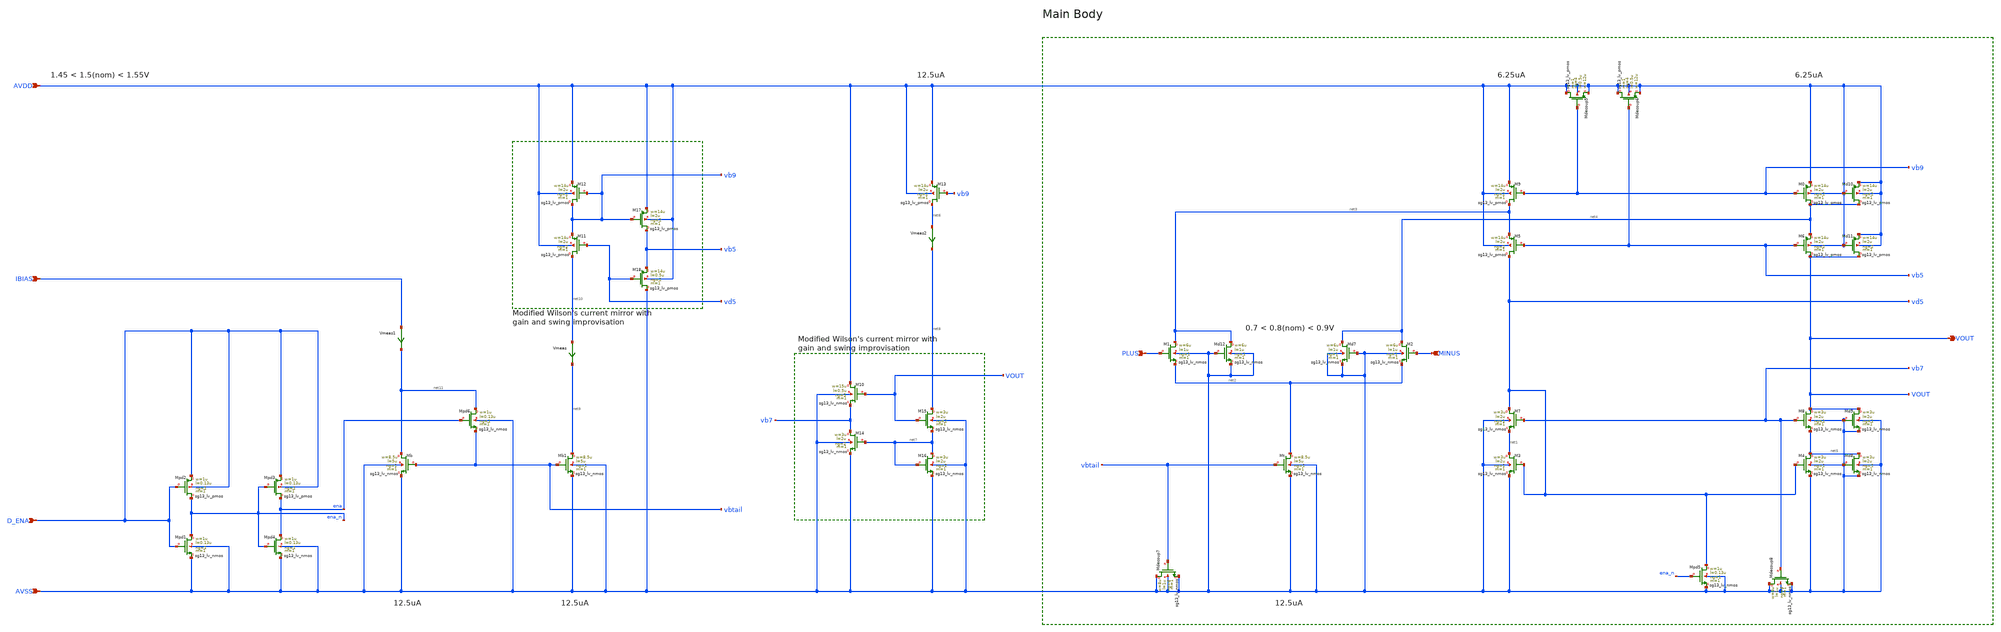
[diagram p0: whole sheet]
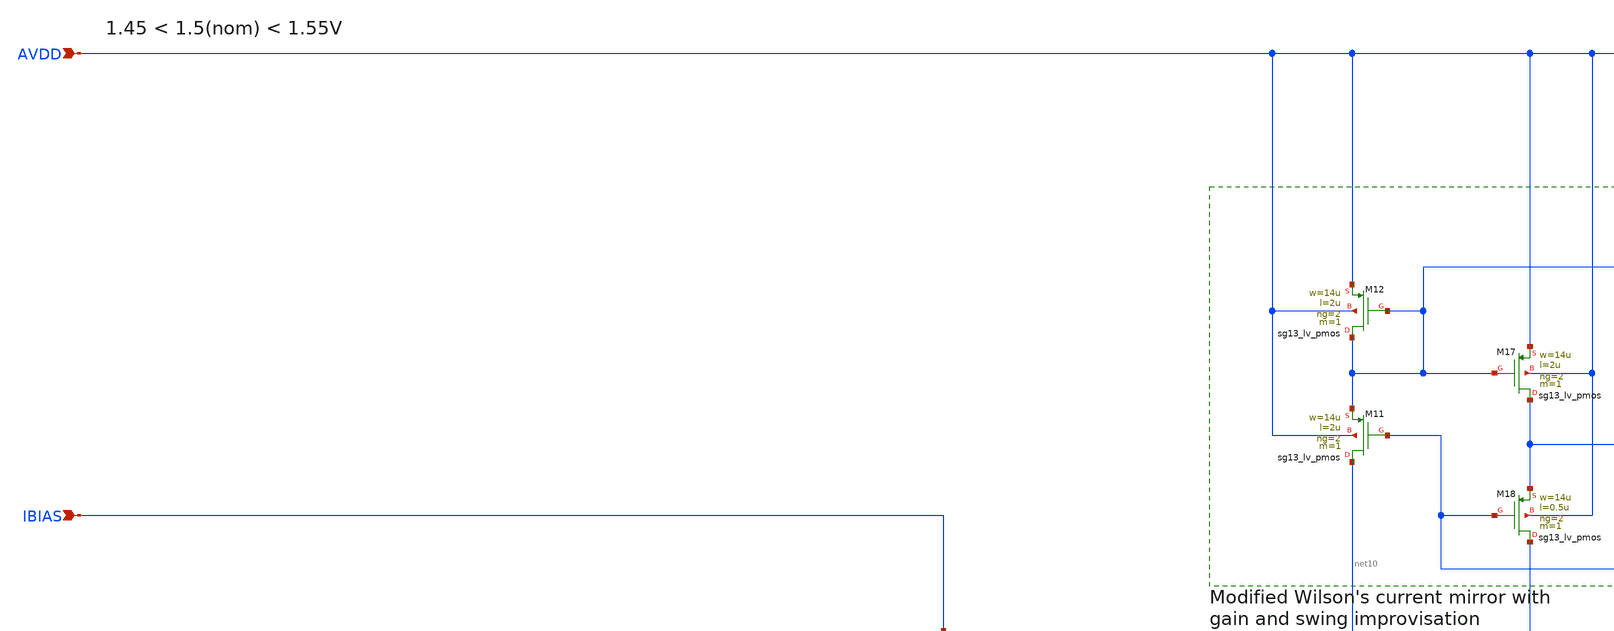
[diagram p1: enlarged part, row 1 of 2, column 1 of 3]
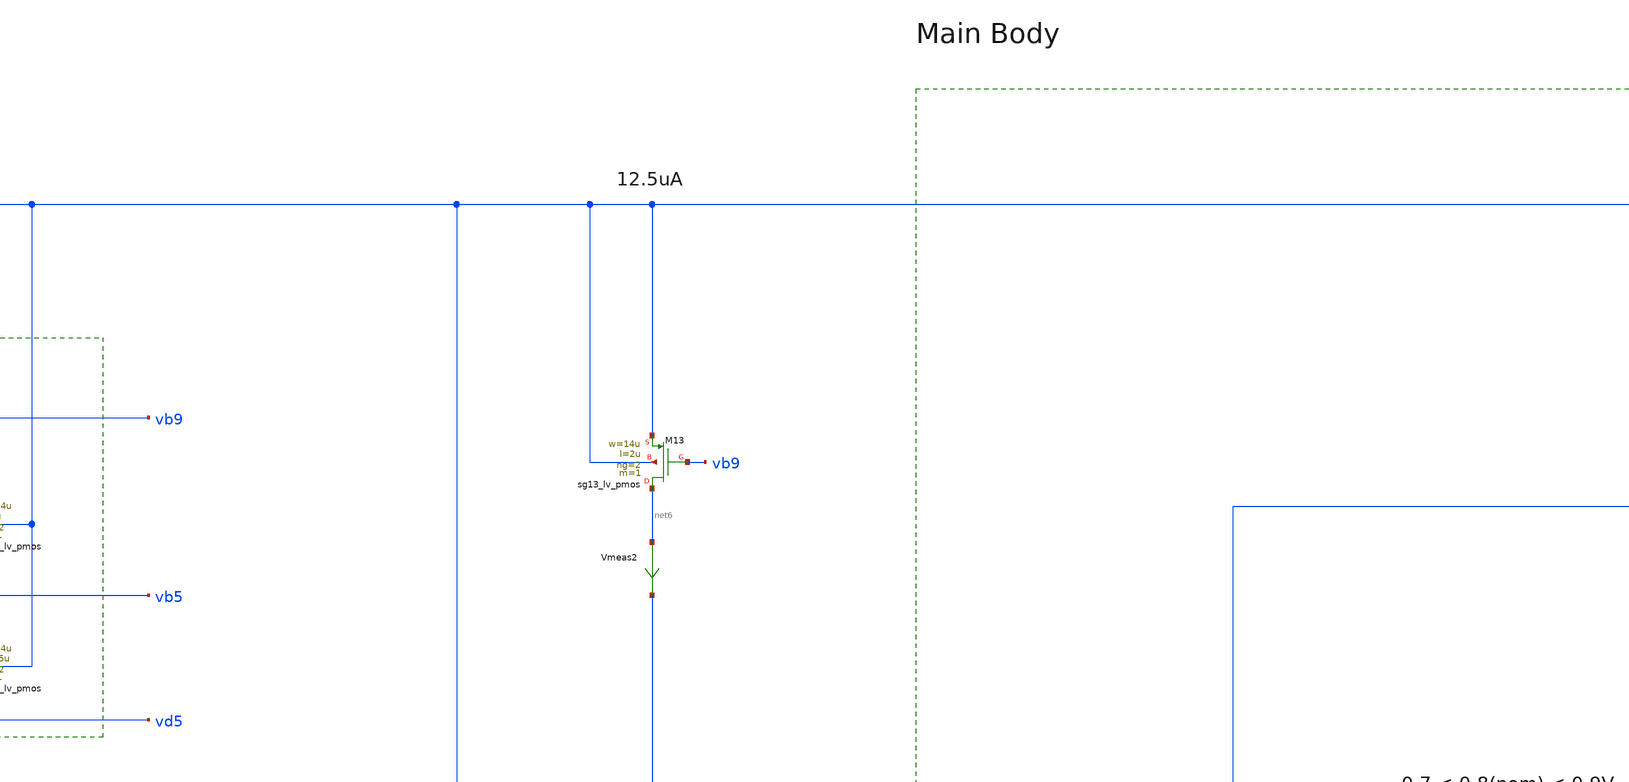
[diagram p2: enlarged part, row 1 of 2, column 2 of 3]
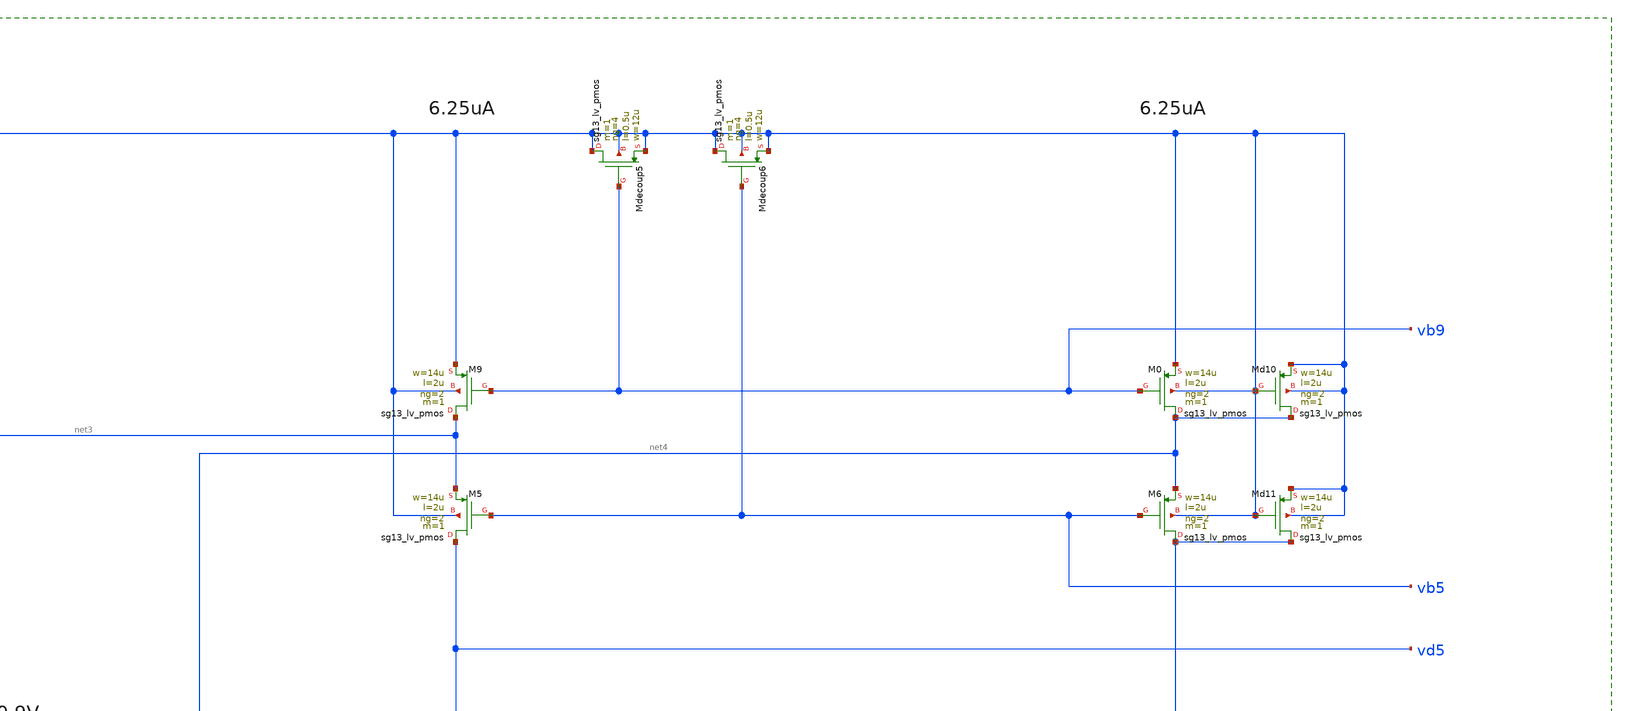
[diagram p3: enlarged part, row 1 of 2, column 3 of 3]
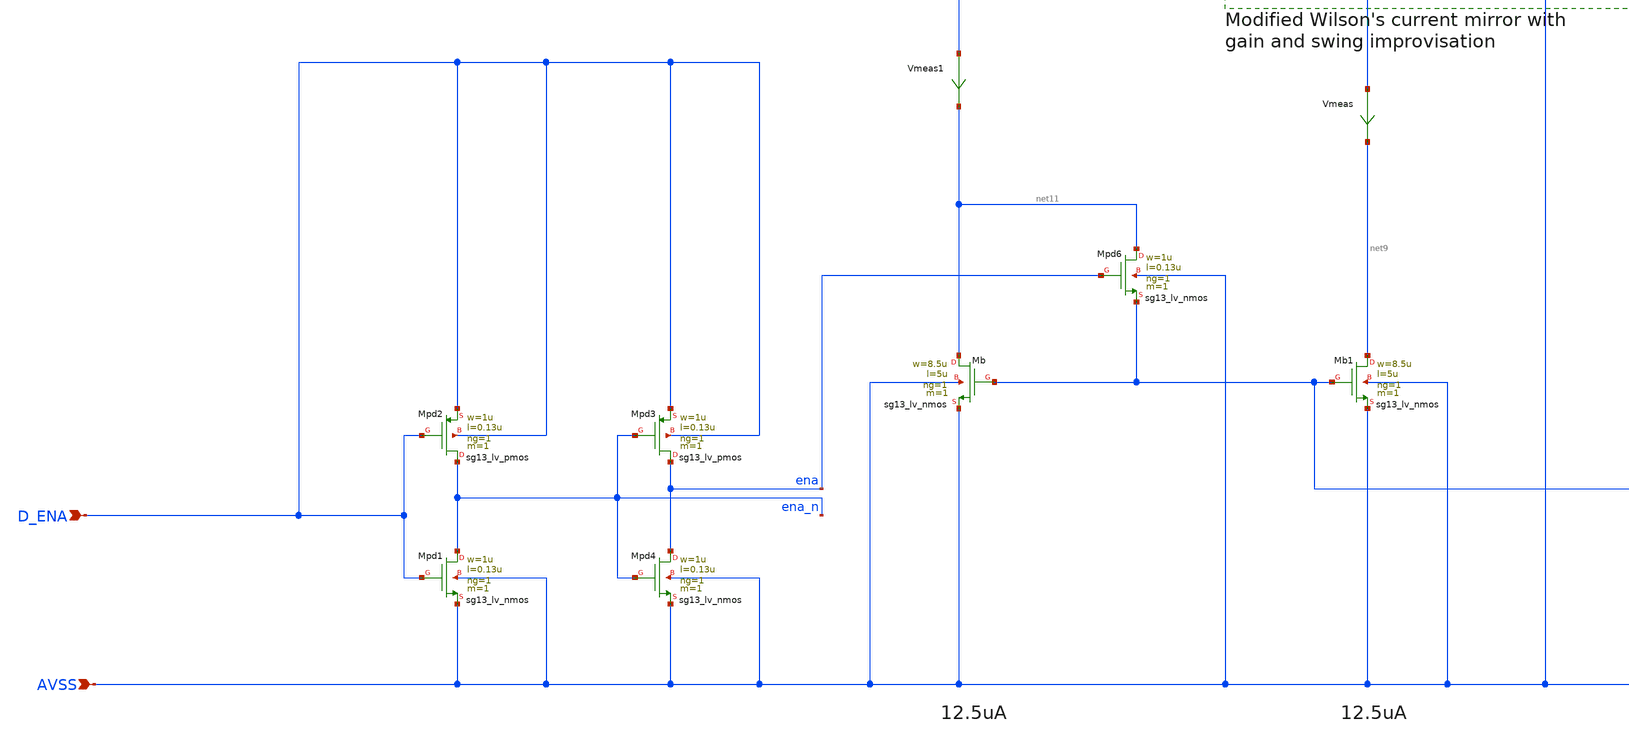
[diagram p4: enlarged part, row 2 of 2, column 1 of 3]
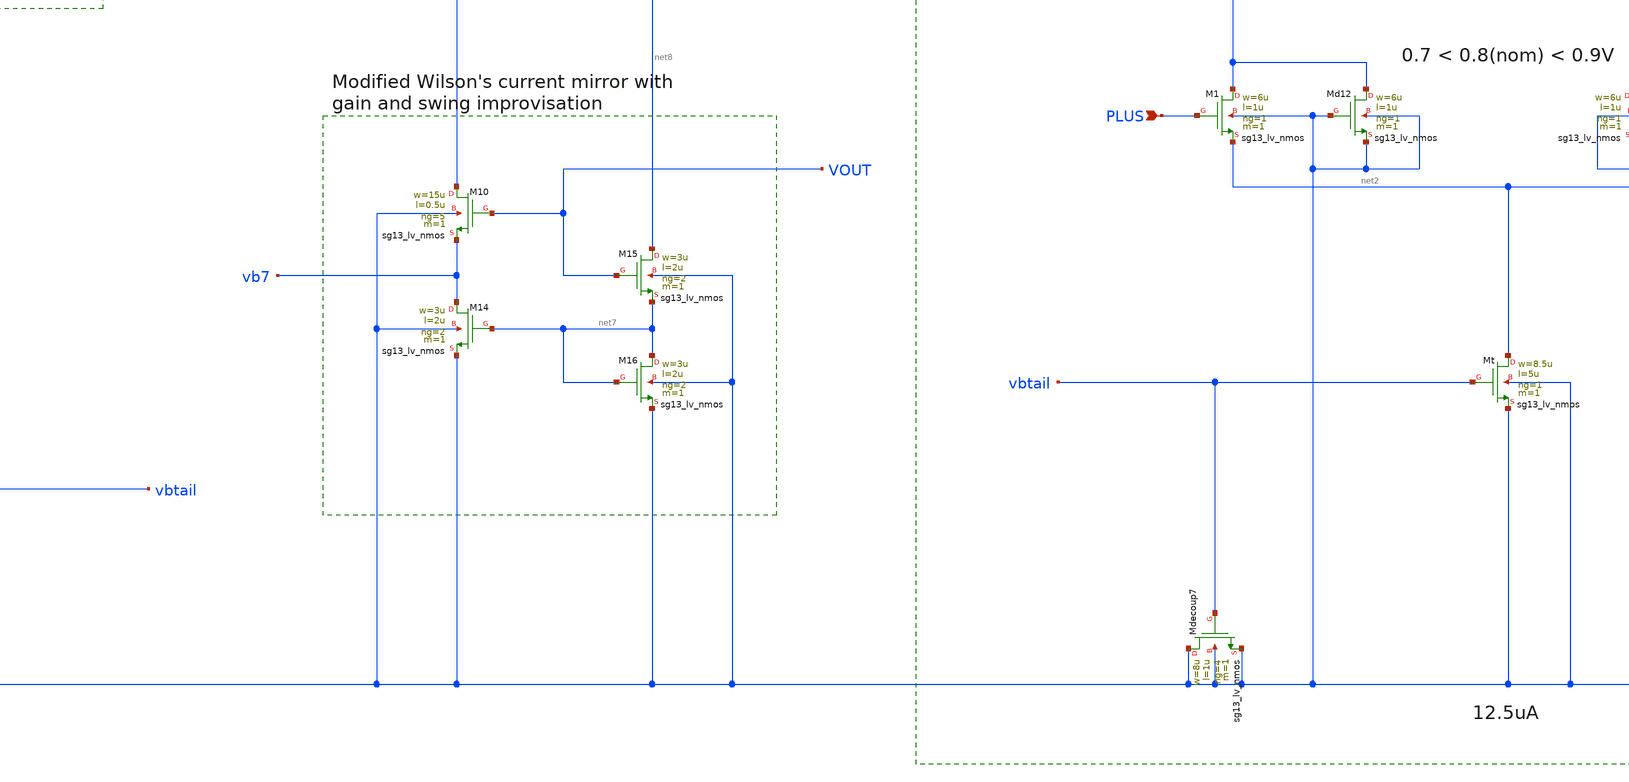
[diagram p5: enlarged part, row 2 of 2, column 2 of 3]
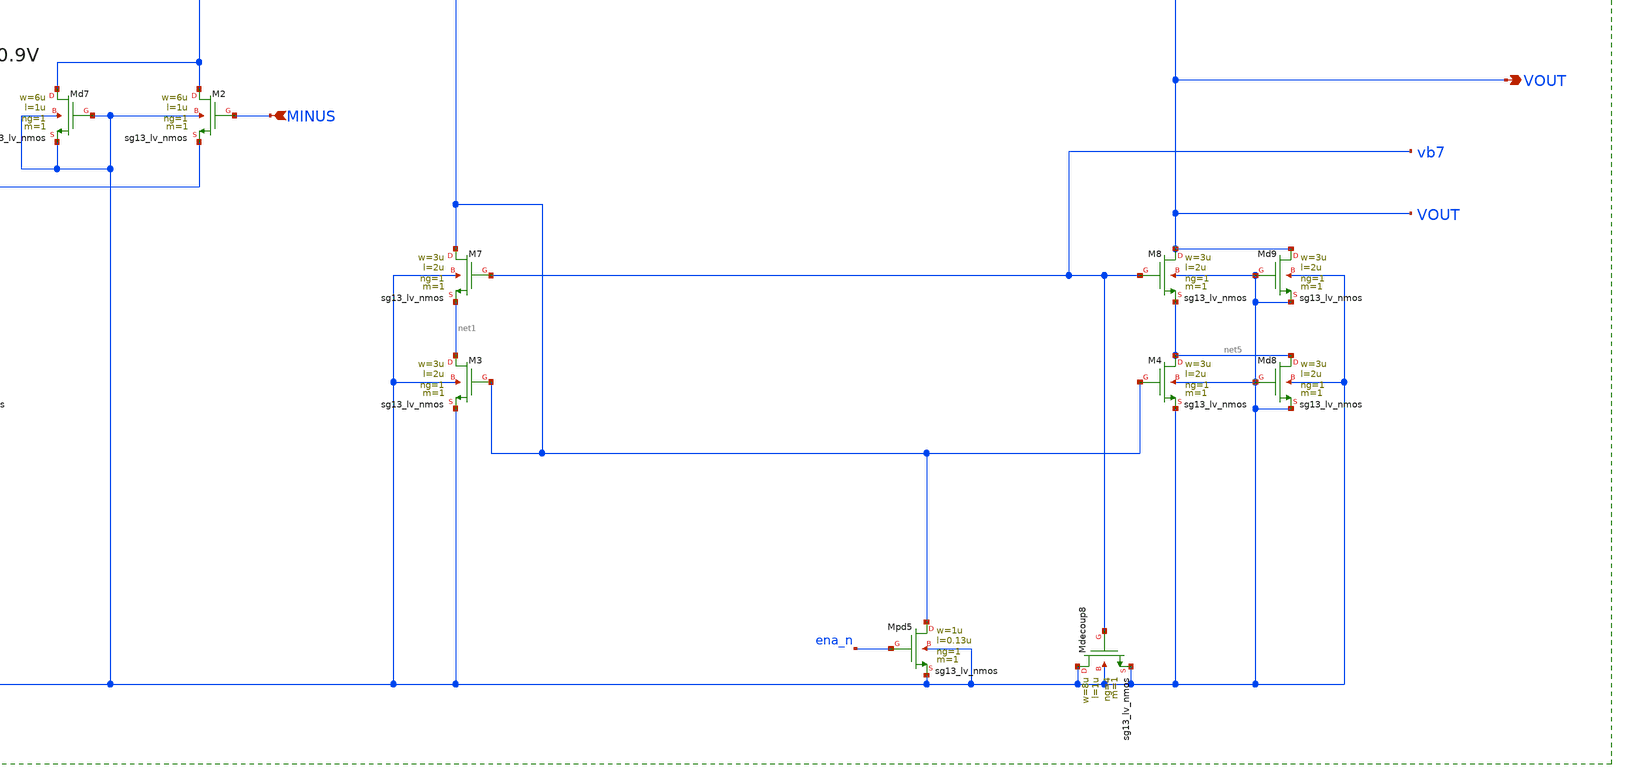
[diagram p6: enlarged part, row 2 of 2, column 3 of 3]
** sch_path: Designs/otas/1_schematics/foldedcascode_nmos.sch
* (c) 2025 Thesis_HP, Apache-2.0 license
**.subckt foldedcascode_nmos VOUT PLUS MINUS AVSS IBIAS AVDD D_ENA
*.opin VOUT
*.ipin PLUS
*.ipin MINUS
*.ipin AVSS
*.ipin IBIAS
*.ipin AVDD
*.ipin D_ENA
XM9 net3 vb9 AVDD AVDD sg13_lv_pmos w=14u l=2u ng=2 m=1 mm_ok=1
XM5 vd5 vb5 net3 AVDD sg13_lv_pmos w=14u l=2u ng=2 m=1 mm_ok=1
XM7 vd5 vb7 net1 AVSS sg13_lv_nmos w=3u l=2u ng=1 m=1 mm_ok=1
XM3 net1 vd5 AVSS AVSS sg13_lv_nmos w=3u l=2u ng=1 m=1 mm_ok=1
XMt net2 vbtail AVSS AVSS sg13_lv_nmos w=8.5u l=5u ng=1 m=1 mm_ok=1
XM1 net3 PLUS net2 AVSS sg13_lv_nmos w=6u l=1u ng=1 m=1 mm_ok=1
XM2 net4 MINUS net2 AVSS sg13_lv_nmos w=6u l=1u ng=1 m=1 mm_ok=1
XMdecoup5 AVDD vb9 AVDD AVDD sg13_lv_pmos w=12u l=0.5u ng=4 m=1 mm_ok=1
XMdecoup6 AVDD vb5 AVDD AVDD sg13_lv_pmos w=12u l=0.5u ng=4 m=1 mm_ok=1
XMdecoup7 AVSS vbtail AVSS AVSS sg13_lv_nmos w=8u l=1u ng=4 m=1 mm_ok=1
XMd7 net4 AVSS AVSS AVSS sg13_lv_nmos w=6u l=1u ng=1 m=1 mm_ok=1
XM6 VOUT vb5 net4 AVDD sg13_lv_pmos w=14u l=2u ng=2 m=1 mm_ok=1
XM0 net4 vb9 AVDD AVDD sg13_lv_pmos w=14u l=2u ng=2 m=1 mm_ok=1
XM8 VOUT vb7 net5 AVSS sg13_lv_nmos w=3u l=2u ng=1 m=1 mm_ok=1
XM4 net5 vd5 AVSS AVSS sg13_lv_nmos w=3u l=2u ng=1 m=1 mm_ok=1
XMd8 net5 AVSS AVSS AVSS sg13_lv_nmos w=3u l=2u ng=1 m=1 mm_ok=1
XMd9 VOUT AVSS AVSS AVSS sg13_lv_nmos w=3u l=2u ng=1 m=1 mm_ok=1
XMd10 net4 AVDD AVDD AVDD sg13_lv_pmos w=14u l=2u ng=2 m=1 mm_ok=1
XMd11 VOUT AVDD AVDD AVDD sg13_lv_pmos w=14u l=2u ng=2 m=1 mm_ok=1
XMpd5 vd5 ena_n AVSS AVSS sg13_lv_nmos w=1u l=0.13u ng=1 m=1 mm_ok=1
XMd12 net3 AVSS AVSS AVSS sg13_lv_nmos w=6u l=1u ng=1 m=1 mm_ok=1
XMdecoup8 AVSS vb7 AVSS AVSS sg13_lv_nmos w=8u l=1u ng=4 m=1 mm_ok=1
XM13 net6 vb9 AVDD AVDD sg13_lv_pmos w=14u l=2u ng=2 m=1 mm_ok=1
Vmeas2 net6 net8 0
.save i(vmeas2)
XM15 net8 VOUT net7 AVSS sg13_lv_nmos w=3u l=2u ng=2 m=1 mm_ok=1
XM16 net7 net7 AVSS AVSS sg13_lv_nmos w=3u l=2u ng=2 m=1 mm_ok=1
XM14 vb7 net7 AVSS AVSS sg13_lv_nmos w=3u l=2u ng=2 m=1 mm_ok=1
XM10 AVDD VOUT vb7 AVSS sg13_lv_nmos w=15u l=0.5u ng=5 m=1 mm_ok=1
XMb net11 vbtail AVSS AVSS sg13_lv_nmos w=8.5u l=5u ng=1 m=1 mm_ok=1
XMpd6 net11 ena vbtail AVSS sg13_lv_nmos w=1u l=0.13u ng=1 m=1 mm_ok=1
XMb1 net9 vbtail AVSS AVSS sg13_lv_nmos w=8.5u l=5u ng=1 m=1 mm_ok=1
Vmeas net10 net9 0
.save i(vmeas)
XM11 net10 vd5 vb9 AVDD sg13_lv_pmos w=14u l=2u ng=2 m=1 mm_ok=1
XM12 vb9 vb9 AVDD AVDD sg13_lv_pmos w=14u l=2u ng=2 m=1 mm_ok=1
XM18 AVSS vd5 vb5 AVDD sg13_lv_pmos w=14u l=0.5u ng=2 m=1 mm_ok=1
XM17 vb5 vb9 AVDD AVDD sg13_lv_pmos w=14u l=2u ng=2 m=1 mm_ok=1
XMpd2 ena_n D_ENA D_ENA D_ENA sg13_lv_pmos w=1u l=0.13u ng=1 m=1 mm_ok=1
Vmeas1 IBIAS net11 0
.save i(vmeas1)
XMpd3 ena ena_n D_ENA D_ENA sg13_lv_pmos w=1u l=0.13u ng=1 m=1 mm_ok=1
XMpd1 ena_n D_ENA AVSS AVSS sg13_lv_nmos w=1u l=0.13u ng=1 m=1 mm_ok=1
XMpd4 ena ena_n AVSS AVSS sg13_lv_nmos w=1u l=0.13u ng=1 m=1 mm_ok=1
**.ends
.end
